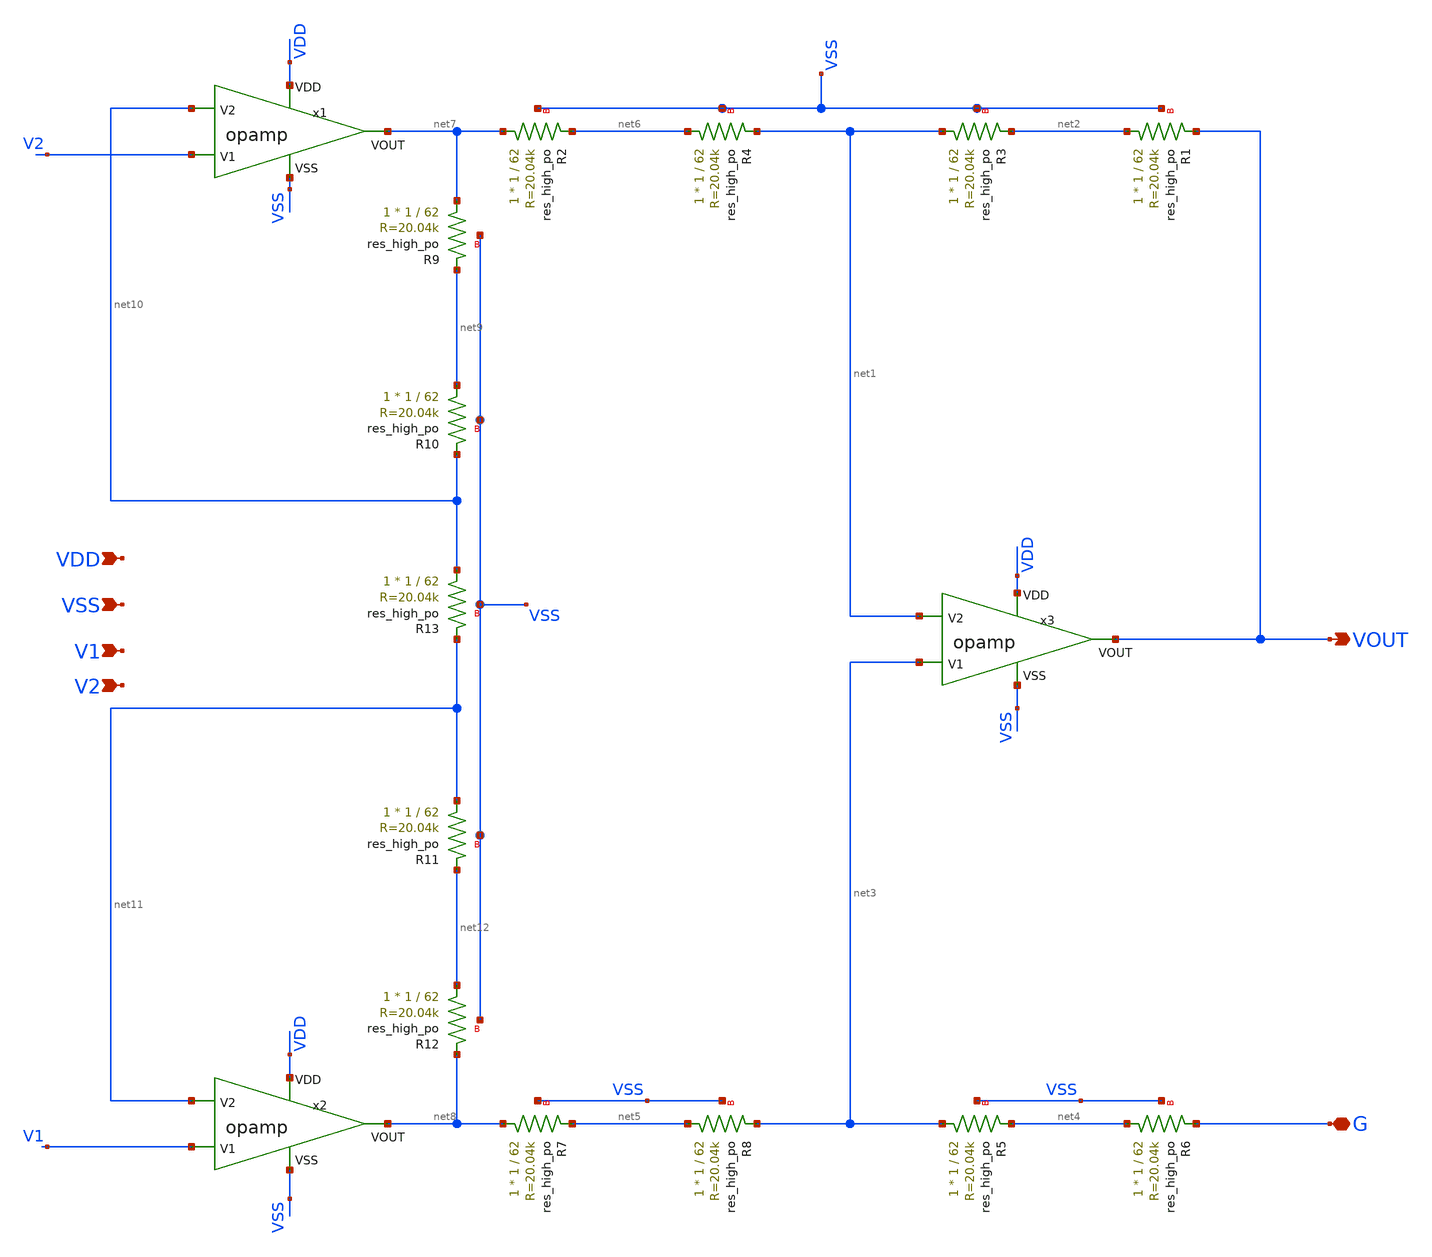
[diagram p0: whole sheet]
** sch_path: xschem/IA.sch
**.subckt IA VOUT G VDD VSS V1 V2
*.opin VOUT
*.iopin G
*.ipin VDD
*.ipin VSS
*.ipin V1
*.ipin V2
XR3 net1 net2 VSS sky130_fd_pr__res_high_po W=1 L=62 mult=1 m=1
XR1 net2 VOUT VSS sky130_fd_pr__res_high_po W=1 L=62 mult=1 m=1
XR2 net7 net6 VSS sky130_fd_pr__res_high_po W=1 L=62 mult=1 m=1
XR4 net6 net1 VSS sky130_fd_pr__res_high_po W=1 L=62 mult=1 m=1
XR5 net3 net4 VSS sky130_fd_pr__res_high_po W=1 L=62 mult=1 m=1
XR6 net4 G VSS sky130_fd_pr__res_high_po W=1 L=62 mult=1 m=1
XR7 net8 net5 VSS sky130_fd_pr__res_high_po W=1 L=62 mult=1 m=1
XR8 net5 net3 VSS sky130_fd_pr__res_high_po W=1 L=62 mult=1 m=1
XR9 net7 net9 VSS sky130_fd_pr__res_high_po W=1 L=62 mult=1 m=1
XR10 net9 net10 VSS sky130_fd_pr__res_high_po W=1 L=62 mult=1 m=1
XR11 net11 net12 VSS sky130_fd_pr__res_high_po W=1 L=62 mult=1 m=1
XR12 net12 net8 VSS sky130_fd_pr__res_high_po W=1 L=62 mult=1 m=1
XR13 net10 net11 VSS sky130_fd_pr__res_high_po W=1 L=62 mult=1 m=1
x1 VDD VSS V2 net10 net7 opamp
x2 VDD VSS V1 net11 net8 opamp
x3 VDD VSS net3 net1 VOUT opamp
**.ends

* expanding   symbol:  /foss/designs/chipalooza2024/sky130_hcmus_ip__instramp/xschem/opamp.sym # of
*+ pins=5
** sym_path: xschem/opamp.sym
** sch_path: xschem/opamp.sch
.subckt opamp VDD VSS V1 V2 VOUT
*.ipin VSS
*.ipin VDD
*.ipin V2
*.ipin V1
*.opin VOUT
XM2 net5 V2 net1 VSS sky130_fd_pr__nfet_01v8 L=1 W=8.5 nf=1 ad='int((nf+1)/2) * W/nf * 0.29' as='int((nf+2)/2) * W/nf * 0.29'
+ pd='2*int((nf+1)/2) * (W/nf + 0.29)' ps='2*int((nf+2)/2) * (W/nf + 0.29)' nrd='0.29 / W' nrs='0.29 / W'
+ sa=0 sb=0 sd=0 mult=1 m=1
XM1 net6 net5 VDD VDD sky130_fd_pr__pfet_01v8 L=1 W=41 nf=1 ad='int((nf+1)/2) * W/nf * 0.29' as='int((nf+2)/2) * W/nf * 0.29'
+ pd='2*int((nf+1)/2) * (W/nf + 0.29)' ps='2*int((nf+2)/2) * (W/nf + 0.29)' nrd='0.29 / W' nrs='0.29 / W'
+ sa=0 sb=0 sd=0 mult=1 m=1
XM4 net6 V1 net1 VSS sky130_fd_pr__nfet_01v8 L=1 W=8.5 nf=1 ad='int((nf+1)/2) * W/nf * 0.29' as='int((nf+2)/2) * W/nf * 0.29'
+ pd='2*int((nf+1)/2) * (W/nf + 0.29)' ps='2*int((nf+2)/2) * (W/nf + 0.29)' nrd='0.29 / W' nrs='0.29 / W'
+ sa=0 sb=0 sd=0 mult=1 m=1
XM5 net1 net4 VSS VSS sky130_fd_pr__nfet_01v8 L=1 W=20 nf=1 ad='int((nf+1)/2) * W/nf * 0.29' as='int((nf+2)/2) * W/nf * 0.29'
+ pd='2*int((nf+1)/2) * (W/nf + 0.29)' ps='2*int((nf+2)/2) * (W/nf + 0.29)' nrd='0.29 / W' nrs='0.29 / W'
+ sa=0 sb=0 sd=0 mult=1 m=1
XM6 VOUT net4 VSS VSS sky130_fd_pr__nfet_01v8 L=1 W=19 nf=1 ad='int((nf+1)/2) * W/nf * 0.29' as='int((nf+2)/2) * W/nf * 0.29'
+ pd='2*int((nf+1)/2) * (W/nf + 0.29)' ps='2*int((nf+2)/2) * (W/nf + 0.29)' nrd='0.29 / W' nrs='0.29 / W'
+ sa=0 sb=0 sd=0 mult=1 m=1
XM7 net4 net4 VSS VSS sky130_fd_pr__nfet_01v8 L=1 W=20 nf=1 ad='int((nf+1)/2) * W/nf * 0.29' as='int((nf+2)/2) * W/nf * 0.29'
+ pd='2*int((nf+1)/2) * (W/nf + 0.29)' ps='2*int((nf+2)/2) * (W/nf + 0.29)' nrd='0.29 / W' nrs='0.29 / W'
+ sa=0 sb=0 sd=0 mult=1 m=1
XM3 net5 net5 VDD VDD sky130_fd_pr__pfet_01v8 L=1 W=41 nf=1 ad='int((nf+1)/2) * W/nf * 0.29' as='int((nf+2)/2) * W/nf * 0.29'
+ pd='2*int((nf+1)/2) * (W/nf + 0.29)' ps='2*int((nf+2)/2) * (W/nf + 0.29)' nrd='0.29 / W' nrs='0.29 / W'
+ sa=0 sb=0 sd=0 mult=1 m=1
XM8 VOUT net6 VDD VDD sky130_fd_pr__pfet_01v8 L=1 W=40 nf=1 ad='int((nf+1)/2) * W/nf * 0.29' as='int((nf+2)/2) * W/nf * 0.29'
+ pd='2*int((nf+1)/2) * (W/nf + 0.29)' ps='2*int((nf+2)/2) * (W/nf + 0.29)' nrd='0.29 / W' nrs='0.29 / W'
+ sa=0 sb=0 sd=0 mult=2 m=2
XR3 net2 VDD VSS sky130_fd_pr__res_high_po W=1 L=50 mult=1 m=1
XR1 net3 net2 VSS sky130_fd_pr__res_high_po W=1 L=50 mult=1 m=1
XR2 net4 net3 VSS sky130_fd_pr__res_high_po W=1 L=50 mult=1 m=1
XR4 net7 VOUT VSS sky130_fd_pr__res_high_po W=1 L=7 mult=1 m=1
XC1 net7 net6 sky130_fd_pr__cap_mim_m3_1 W=5.55 L=10 MF=20 m=20
.ends

.end
